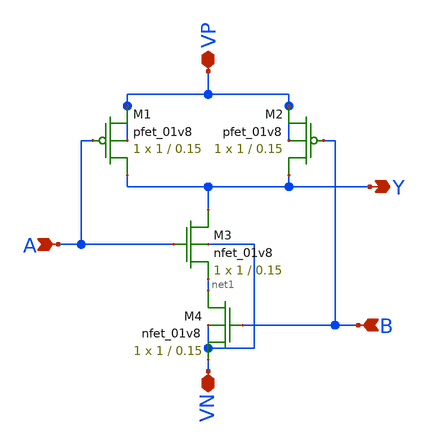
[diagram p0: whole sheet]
** sch_path: MP1/xschem/NAND.sch
**.subckt NAND VP VN A Y B
*.iopin VP
*.iopin VN
*.ipin A
*.opin Y
*.ipin B
XM1 Y A VP VP sky130_fd_pr__pfet_01v8 L=0.15 W=1 nf=1 ad='int((nf+1)/2) * W/nf * 0.29' as='int((nf+2)/2) * W/nf * 0.29'
+ pd='2*int((nf+1)/2) * (W/nf + 0.29)' ps='2*int((nf+2)/2) * (W/nf + 0.29)' nrd='0.29 / W' nrs='0.29 / W'
+ sa=0 sb=0 sd=0 mult=1 m=1
XM2 Y B VP VP sky130_fd_pr__pfet_01v8 L=0.15 W=1 nf=1 ad='int((nf+1)/2) * W/nf * 0.29' as='int((nf+2)/2) * W/nf * 0.29'
+ pd='2*int((nf+1)/2) * (W/nf + 0.29)' ps='2*int((nf+2)/2) * (W/nf + 0.29)' nrd='0.29 / W' nrs='0.29 / W'
+ sa=0 sb=0 sd=0 mult=1 m=1
XM3 Y A net1 VN sky130_fd_pr__nfet_01v8 L=0.15 W=1 nf=1 ad='int((nf+1)/2) * W/nf * 0.29' as='int((nf+2)/2) * W/nf * 0.29'
+ pd='2*int((nf+1)/2) * (W/nf + 0.29)' ps='2*int((nf+2)/2) * (W/nf + 0.29)' nrd='0.29 / W' nrs='0.29 / W'
+ sa=0 sb=0 sd=0 mult=1 m=1
XM4 net1 B VN VN sky130_fd_pr__nfet_01v8 L=0.15 W=1 nf=1 ad='int((nf+1)/2) * W/nf * 0.29' as='int((nf+2)/2) * W/nf * 0.29'
+ pd='2*int((nf+1)/2) * (W/nf + 0.29)' ps='2*int((nf+2)/2) * (W/nf + 0.29)' nrd='0.29 / W' nrs='0.29 / W'
+ sa=0 sb=0 sd=0 mult=1 m=1
**.ends
.end
